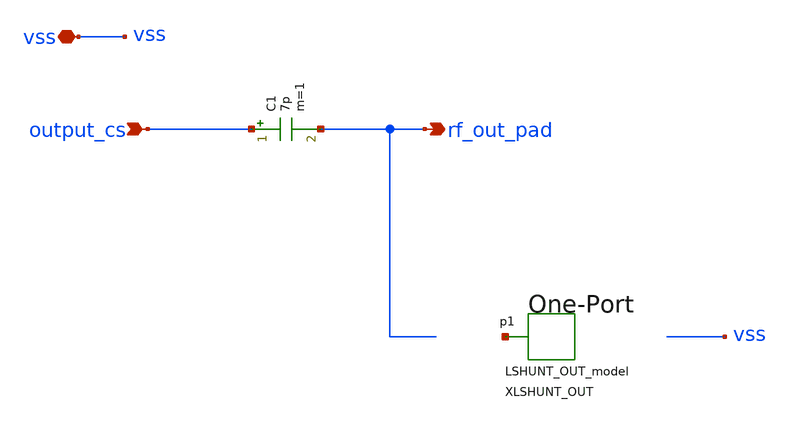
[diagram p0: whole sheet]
** sch_path: xschem/lna_core_output_match.sch
**.subckt lna_core_output_match output_cs vss rf_out_pad
*.ipin output_cs
*.iopin vss
*.opin rf_out_pad
C1 output_cs rf_out_pad 7p m=1
XLSHUNT_OUT net1 LSHUNT_OUT_model
**.ends
.end
